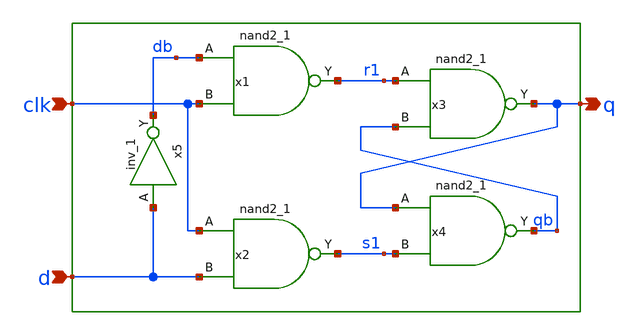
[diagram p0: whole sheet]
** sch_path: src/xe/test_cases/rs_nand_latch.sch
**.subckt rs_nand_latch clk d q
*.ipin clk
*.ipin d
*.opin q
x1 db clk vss vss vcc vcc r1 sky130_fd_sc_hd__nand2_1
x5 d vss vss vcc vcc db sky130_fd_sc_hd__inv_1
x2 clk d vss vss vcc vcc s1 sky130_fd_sc_hd__nand2_1
x3 r1 qb vss vss vcc vcc q sky130_fd_sc_hd__nand2_1
x4 q s1 vss vss vcc vcc qb sky130_fd_sc_hd__nand2_1
**.ends
.end
